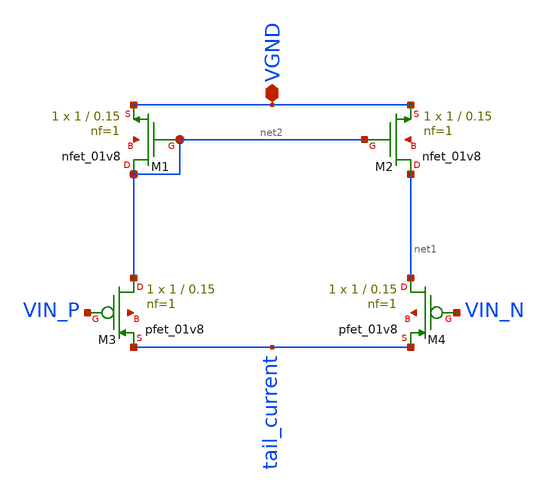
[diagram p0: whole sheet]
** sch_path: xschem/5t_ota.sch
**.subckt 5t_ota VGND
*.iopin VGND
XM1 net2 net2 VGND net3 sky130_fd_pr__nfet_01v8 L=0.15 W=1 nf=1 ad='int((1 + 1)/2) * 1 / 1 * 0.29' as='int((1 + 2)/2) * 1 / 1 * 0.29'
+ pd='2*int((1 + 1)/2) * (1 / 1 + 0.29)' ps='2*int((1 + 2)/2) * (1 / 1 + 0.29)' nrd='0.29 / 1 ' nrs='0.29 / 1 '
+ sa=0 sb=0 sd=0 mult=1 m=1
XM2 net1 net2 VGND net4 sky130_fd_pr__nfet_01v8 L=0.15 W=1 nf=1 ad='int((1 + 1)/2) * 1 / 1 * 0.29' as='int((1 + 2)/2) * 1 / 1 * 0.29'
+ pd='2*int((1 + 1)/2) * (1 / 1 + 0.29)' ps='2*int((1 + 2)/2) * (1 / 1 + 0.29)' nrd='0.29 / 1 ' nrs='0.29 / 1 '
+ sa=0 sb=0 sd=0 mult=1 m=1
XM3 net2 VIN_P tail_current net5 sky130_fd_pr__pfet_01v8 L=0.15 W=1 nf=1 ad='int((1 + 1)/2) * 1 / 1 * 0.29'
+ as='int((1 + 2)/2) * 1 / 1 * 0.29' pd='2*int((1 + 1)/2) * (1 / 1 + 0.29)' ps='2*int((1 + 2)/2) * (1 / 1 + 0.29)'
+ nrd='0.29 / 1 ' nrs='0.29 / 1 ' sa=0 sb=0 sd=0 mult=1 m=1
XM4 net1 VIN_N tail_current net6 sky130_fd_pr__pfet_01v8 L=0.15 W=1 nf=1 ad='int((1 + 1)/2) * 1 / 1 * 0.29'
+ as='int((1 + 2)/2) * 1 / 1 * 0.29' pd='2*int((1 + 1)/2) * (1 / 1 + 0.29)' ps='2*int((1 + 2)/2) * (1 / 1 + 0.29)'
+ nrd='0.29 / 1 ' nrs='0.29 / 1 ' sa=0 sb=0 sd=0 mult=1 m=1
**.ends
.end
